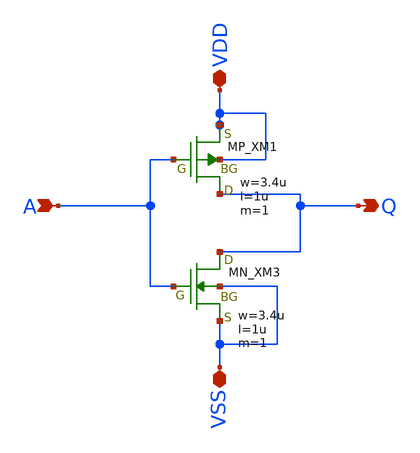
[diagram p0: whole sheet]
** sch_path: inverter/inverter_YU_WENJUN.sch
**.subckt inverter_YU_WENJUN Q A VSS VDD
*.opin Q
*.ipin A
*.iopin VSS
*.iopin VDD
XXM1 Q A VDD VDD PMOS w=3.4u l=1u nrd=0 nrs=0 m=1
XXM3 Q A VSS VSS NMOS w=3.4u l=1u nrd=0 nrs=0 m=1
**.ends
.end
